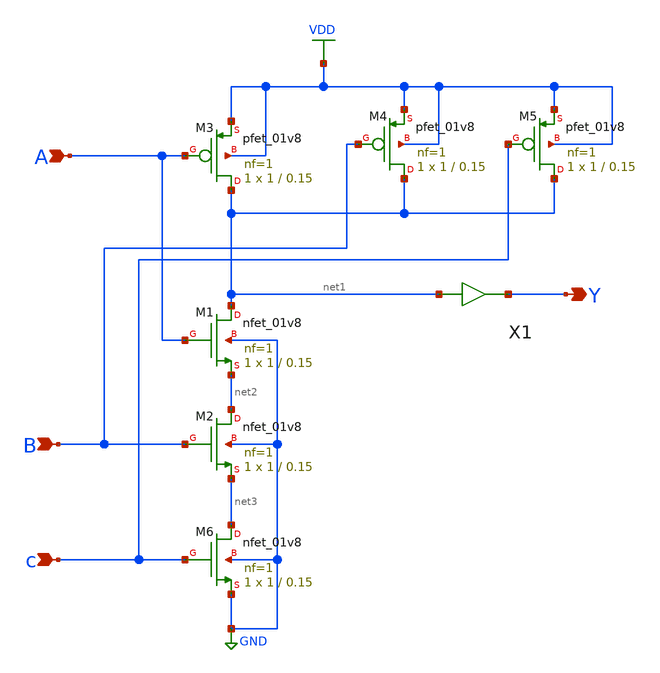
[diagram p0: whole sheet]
** sch_path: gates/AND3.sch
**.subckt AND3 A B Y c
*.ipin A
*.ipin B
*.opin Y
*.ipin c
XM1 net1 A net2 GND sky130_fd_pr__nfet_01v8 L=0.15 W=1 nf=1 ad='int((nf+1)/2) * W/nf * 0.29' as='int((nf+2)/2) * W/nf * 0.29'
+ pd='2*int((nf+1)/2) * (W/nf + 0.29)' ps='2*int((nf+2)/2) * (W/nf + 0.29)' nrd='0.29 / W' nrs='0.29 / W'
+ sa=0 sb=0 sd=0 mult=1 m=1
XM2 net2 B net3 GND sky130_fd_pr__nfet_01v8 L=0.15 W=1 nf=1 ad='int((nf+1)/2) * W/nf * 0.29' as='int((nf+2)/2) * W/nf * 0.29'
+ pd='2*int((nf+1)/2) * (W/nf + 0.29)' ps='2*int((nf+2)/2) * (W/nf + 0.29)' nrd='0.29 / W' nrs='0.29 / W'
+ sa=0 sb=0 sd=0 mult=1 m=1
XM3 net1 A VDD VDD sky130_fd_pr__pfet_01v8 L=0.15 W=1 nf=1 ad='int((nf+1)/2) * W/nf * 0.29' as='int((nf+2)/2) * W/nf * 0.29'
+ pd='2*int((nf+1)/2) * (W/nf + 0.29)' ps='2*int((nf+2)/2) * (W/nf + 0.29)' nrd='0.29 / W' nrs='0.29 / W'
+ sa=0 sb=0 sd=0 mult=1 m=1
XM4 net1 B VDD VDD sky130_fd_pr__pfet_01v8 L=0.15 W=1 nf=1 ad='int((nf+1)/2) * W/nf * 0.29' as='int((nf+2)/2) * W/nf * 0.29'
+ pd='2*int((nf+1)/2) * (W/nf + 0.29)' ps='2*int((nf+2)/2) * (W/nf + 0.29)' nrd='0.29 / W' nrs='0.29 / W'
+ sa=0 sb=0 sd=0 mult=1 m=1
XM5 net1 c VDD VDD sky130_fd_pr__pfet_01v8 L=0.15 W=1 nf=1 ad='int((nf+1)/2) * W/nf * 0.29' as='int((nf+2)/2) * W/nf * 0.29'
+ pd='2*int((nf+1)/2) * (W/nf + 0.29)' ps='2*int((nf+2)/2) * (W/nf + 0.29)' nrd='0.29 / W' nrs='0.29 / W'
+ sa=0 sb=0 sd=0 mult=1 m=1
XM6 net3 c GND GND sky130_fd_pr__nfet_01v8 L=0.15 W=1 nf=1 ad='int((nf+1)/2) * W/nf * 0.29' as='int((nf+2)/2) * W/nf * 0.29'
+ pd='2*int((nf+1)/2) * (W/nf + 0.29)' ps='2*int((nf+2)/2) * (W/nf + 0.29)' nrd='0.29 / W' nrs='0.29 / W'
+ sa=0 sb=0 sd=0 mult=1 m=1
X1 net1 Y inv_vtc
**.ends

* expanding   symbol:  /home/apn/test_xschem_sky130/inv_vtc.sym # of pins=2
** sym_path: gates/inv_vtc.sym
** sch_path: gates/inv_vtc.sch
.subckt inv_vtc A Y
*.ipin A
*.opin Y
XM1 Y A VDD VDD sky130_fd_pr__pfet_01v8 L=0.15 W=2 nf=1 ad='int((nf+1)/2) * W/nf * 0.29' as='int((nf+2)/2) * W/nf * 0.29'
+ pd='2*int((nf+1)/2) * (W/nf + 0.29)' ps='2*int((nf+2)/2) * (W/nf + 0.29)' nrd='0.29 / W' nrs='0.29 / W'
+ sa=0 sb=0 sd=0 mult=1 m=1
XM2 Y A GND GND sky130_fd_pr__nfet_01v8 L=0.15 W=1 nf=1 ad='int((nf+1)/2) * W/nf * 0.29' as='int((nf+2)/2) * W/nf * 0.29'
+ pd='2*int((nf+1)/2) * (W/nf + 0.29)' ps='2*int((nf+2)/2) * (W/nf + 0.29)' nrd='0.29 / W' nrs='0.29 / W'
+ sa=0 sb=0 sd=0 mult=1 m=1
.ends

.GLOBAL VDD
.GLOBAL GND
.end
